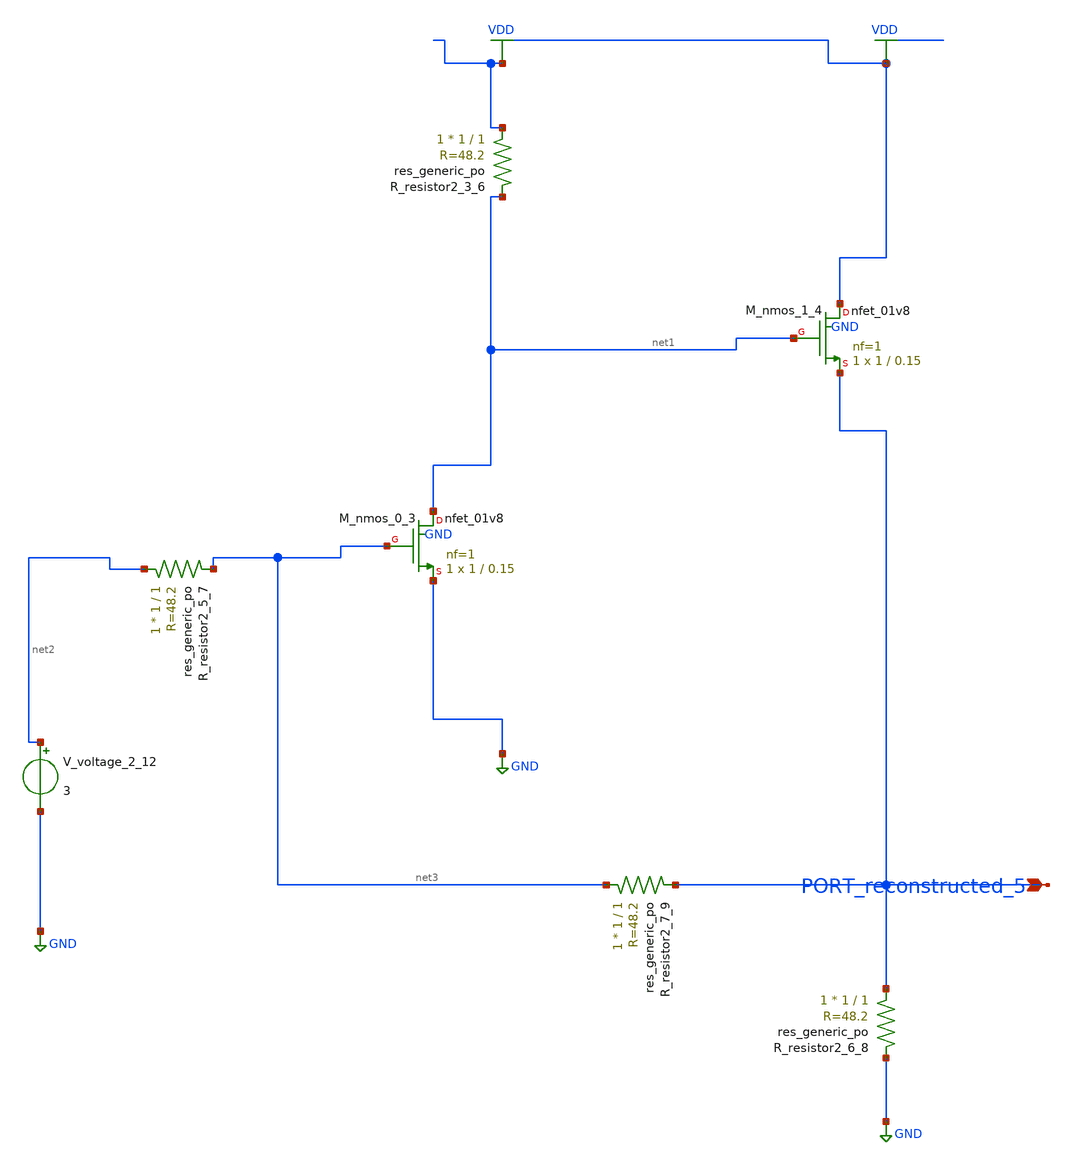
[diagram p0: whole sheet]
** sch_path: schematics/AMSNet/604.sch
**.subckt 604 PORT_reconstructed_5
*.ipin PORT_reconstructed_5
XM_nmos_0_3 net1 net3 GND GND sky130_fd_pr__nfet_01v8 L=0.15 W=1 nf=1 ad='int((1 + 1)/2) * 1 / 1 * 0.29'
+ as='int((1 + 2)/2) * 1 / 1 * 0.29' pd='2*int((1 + 1)/2) * (1 / 1 + 0.29)' ps='2*int((1 + 2)/2) * (1 / 1 + 0.29)'
+ nrd='0.29 / 1 ' nrs='0.29 / 1 ' sa=0 sb=0 sd=0 mult=1 m=1
XM_nmos_1_4 VDD net1 PORT_reconstructed_5 GND sky130_fd_pr__nfet_01v8 L=0.15 W=1 nf=1 ad='int((1 + 1)/2) * 1 / 1 * 0.29'
+ as='int((1 + 2)/2) * 1 / 1 * 0.29' pd='2*int((1 + 1)/2) * (1 / 1 + 0.29)' ps='2*int((1 + 2)/2) * (1 / 1 + 0.29)'
+ nrd='0.29 / 1 ' nrs='0.29 / 1 ' sa=0 sb=0 sd=0 mult=1 m=1
XR_resistor2_3_6 VDD net1 sky130_fd_pr__res_generic_po W=1 L=1 m=1
XR_resistor2_5_7 net2 net3 sky130_fd_pr__res_generic_po W=1 L=1 m=1
XR_resistor2_6_8 PORT_reconstructed_5 GND sky130_fd_pr__res_generic_po W=1 L=1 m=1
XR_resistor2_7_9 net3 PORT_reconstructed_5 sky130_fd_pr__res_generic_po W=1 L=1 m=1
V_voltage_2_12 net2 GND 3
**.ends
.GLOBAL GND
.GLOBAL VDD
.end
